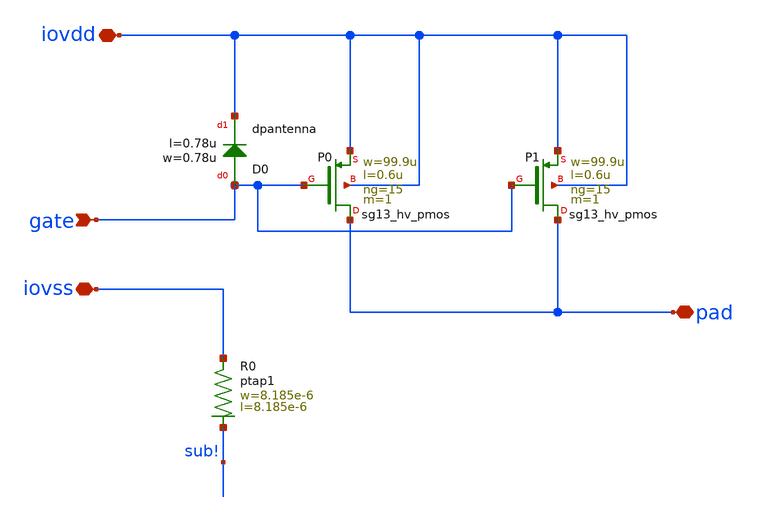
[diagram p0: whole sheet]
** sch_path: ihp-sg13g2/libs.ref/sg13g2_io/sch/xschem/sg13g2_Clamp_P15N15D.sch
**.subckt sg13g2_Clamp_P15N15D iovdd iovss pad gate
*.iopin iovdd
*.iopin iovss
*.iopin pad
*.ipin gate
XP0 pad gate iovdd iovdd sg13_hv_pmos w=99.9u l=0.6u ng=15 m=1 mm_ok=1
XP1 pad gate iovdd iovdd sg13_hv_pmos w=99.9u l=0.6u ng=15 m=1 mm_ok=1
XD0 gate iovdd dpantenna l=0.78u w=0.78u
XR0 iovss sub! ptap1 R=9.826 w=8.185e-6 l=8.185e-6
**.ends
.end
